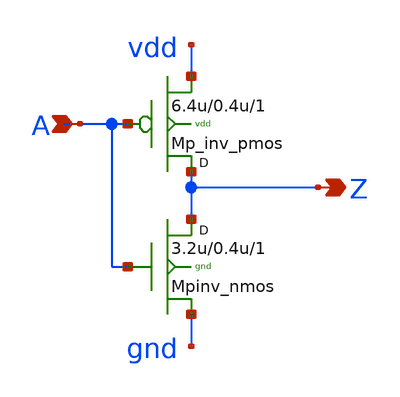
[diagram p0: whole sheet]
** sch_path: sram_2_64_scn4m_lcc/pinv_6.sch
**.subckt pinv_6 A Z
*.ipin A
*.opin Z
Mpinv_nmos Z A gnd gnd n w=3.2u l=0.4u m=1
Mp_inv_pmos Z A vdd vdd p w=6.4u l=0.4u m=1
**.ends
.end
